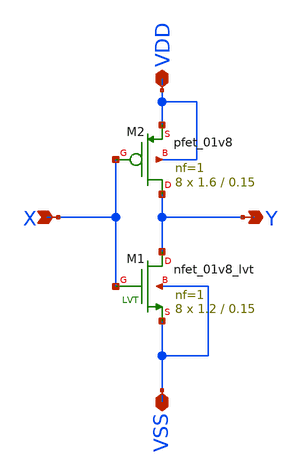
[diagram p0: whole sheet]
** sch_path: xschem_example/inv.sch
**.subckt inv VSS X Y VDD
*.iopin VSS
*.ipin X
*.opin Y
*.iopin VDD
XM1 Y X VSS VSS sky130_fd_pr__nfet_01v8_lvt L=0.15 W=1.2 nf=1 ad='int((nf+1)/2) * W/nf * 0.29' as='int((nf+2)/2) * W/nf * 0.29'
+ pd='2*int((nf+1)/2) * (W/nf + 0.29)' ps='2*int((nf+2)/2) * (W/nf + 0.29)' nrd='0.29 / W' nrs='0.29 / W'
+ sa=0 sb=0 sd=0 mult=8 m=8
XM2 Y X VDD VDD sky130_fd_pr__pfet_01v8 L=0.15 W=1.6 nf=1 ad='int((nf+1)/2) * W/nf * 0.29' as='int((nf+2)/2) * W/nf * 0.29'
+ pd='2*int((nf+1)/2) * (W/nf + 0.29)' ps='2*int((nf+2)/2) * (W/nf + 0.29)' nrd='0.29 / W' nrs='0.29 / W'
+ sa=0 sb=0 sd=0 mult=8 m=8
**.ends
.end
